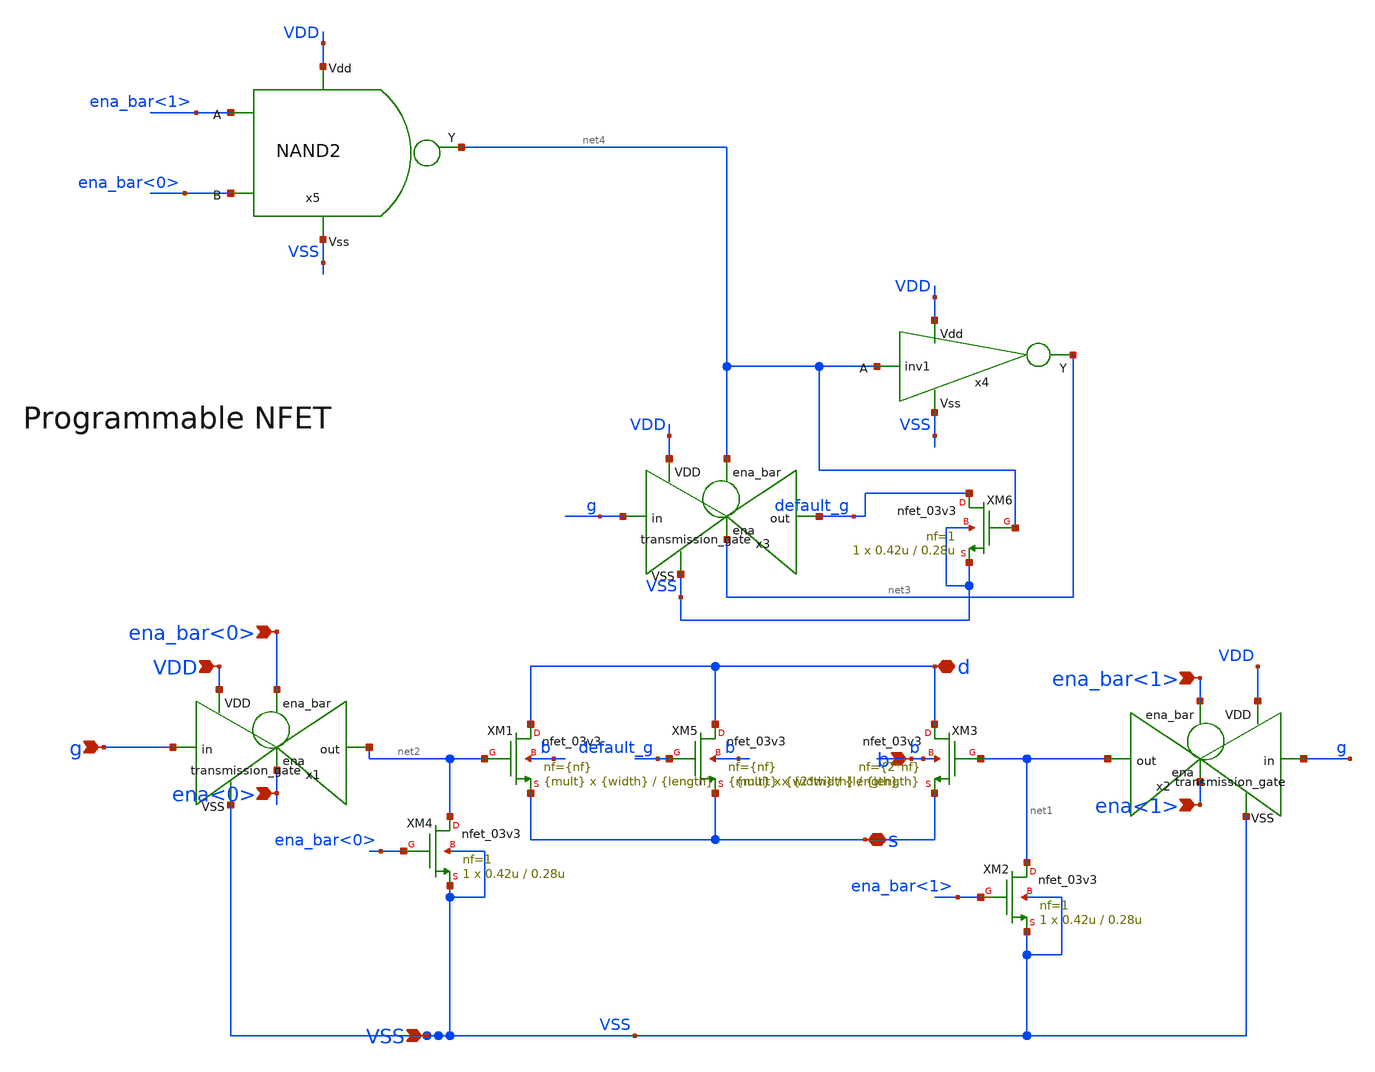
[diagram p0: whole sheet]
** sch_path: designs/libs/core_digital/schem/programmable_nfet.sch
**.subckt programmable_nfet VSS VDD g ena_bar<1> ena_bar<0> ena<1> ena<0> d s b
*.ipin VSS
*.ipin VDD
*.ipin g
*.ipin ena_bar<1>
*.ipin ena_bar<0>
*.ipin ena<1>
*.ipin ena<0>
*.iopin d
*.iopin s
*.ipin b
XM1 d net2 s b nfet_03v3 L={length} W={width} nf={nf} ad='int((nf+1)/2) * W/nf * 0.18u' as='int((nf+2)/2) * W/nf * 0.18u'
+ pd='2*int((nf+1)/2) * (W/nf + 0.18u)' ps='2*int((nf+2)/2) * (W/nf + 0.18u)' nrd='0.18u / W' nrs='0.18u / W'
+ sa=0 sb=0 sd=0 m={mult}
XM3 d net1 s b nfet_03v3 L={length} W={2*width} nf={2*nf} ad='int((nf+1)/2) * W/nf * 0.18u' as='int((nf+2)/2) * W/nf * 0.18u'
+ pd='2*int((nf+1)/2) * (W/nf + 0.18u)' ps='2*int((nf+2)/2) * (W/nf + 0.18u)' nrd='0.18u / W' nrs='0.18u / W'
+ sa=0 sb=0 sd=0 m={mult}
XM2 net1 ena_bar<1> VSS VSS nfet_03v3 L=0.28u W=0.42u nf=1 ad='int((nf+1)/2) * W/nf * 0.18u' as='int((nf+2)/2) * W/nf * 0.18u'
+ pd='2*int((nf+1)/2) * (W/nf + 0.18u)' ps='2*int((nf+2)/2) * (W/nf + 0.18u)' nrd='0.18u / W' nrs='0.18u / W'
+ sa=0 sb=0 sd=0 m=1
XM4 net2 ena_bar<0> VSS VSS nfet_03v3 L=0.28u W=0.42u nf=1 ad='int((nf+1)/2) * W/nf * 0.18u' as='int((nf+2)/2) * W/nf * 0.18u'
+ pd='2*int((nf+1)/2) * (W/nf + 0.18u)' ps='2*int((nf+2)/2) * (W/nf + 0.18u)' nrd='0.18u / W' nrs='0.18u / W'
+ sa=0 sb=0 sd=0 m=1
x1 ena_bar<0> VDD net2 g VSS ena<0> transmission_gate
x2 ena_bar<1> VDD net1 g VSS ena<1> transmission_gate
XM5 d default_g s b nfet_03v3 L={length} W={width} nf={nf} ad='int((nf+1)/2) * W/nf * 0.18u' as='int((nf+2)/2) * W/nf * 0.18u'
+ pd='2*int((nf+1)/2) * (W/nf + 0.18u)' ps='2*int((nf+2)/2) * (W/nf + 0.18u)' nrd='0.18u / W' nrs='0.18u / W'
+ sa=0 sb=0 sd=0 m={mult}
x3 net4 VDD default_g g VSS net3 transmission_gate
x5 VDD net4 ena_bar<1> ena_bar<0> VSS NAND2
x4 VDD net4 net3 VSS inv1
XM6 default_g net4 VSS VSS nfet_03v3 L=0.28u W=0.42u nf=1 ad='int((nf+1)/2) * W/nf * 0.18u' as='int((nf+2)/2) * W/nf * 0.18u'
+ pd='2*int((nf+1)/2) * (W/nf + 0.18u)' ps='2*int((nf+2)/2) * (W/nf + 0.18u)' nrd='0.18u / W' nrs='0.18u / W'
+ sa=0 sb=0 sd=0 m=1
**.ends
.end
